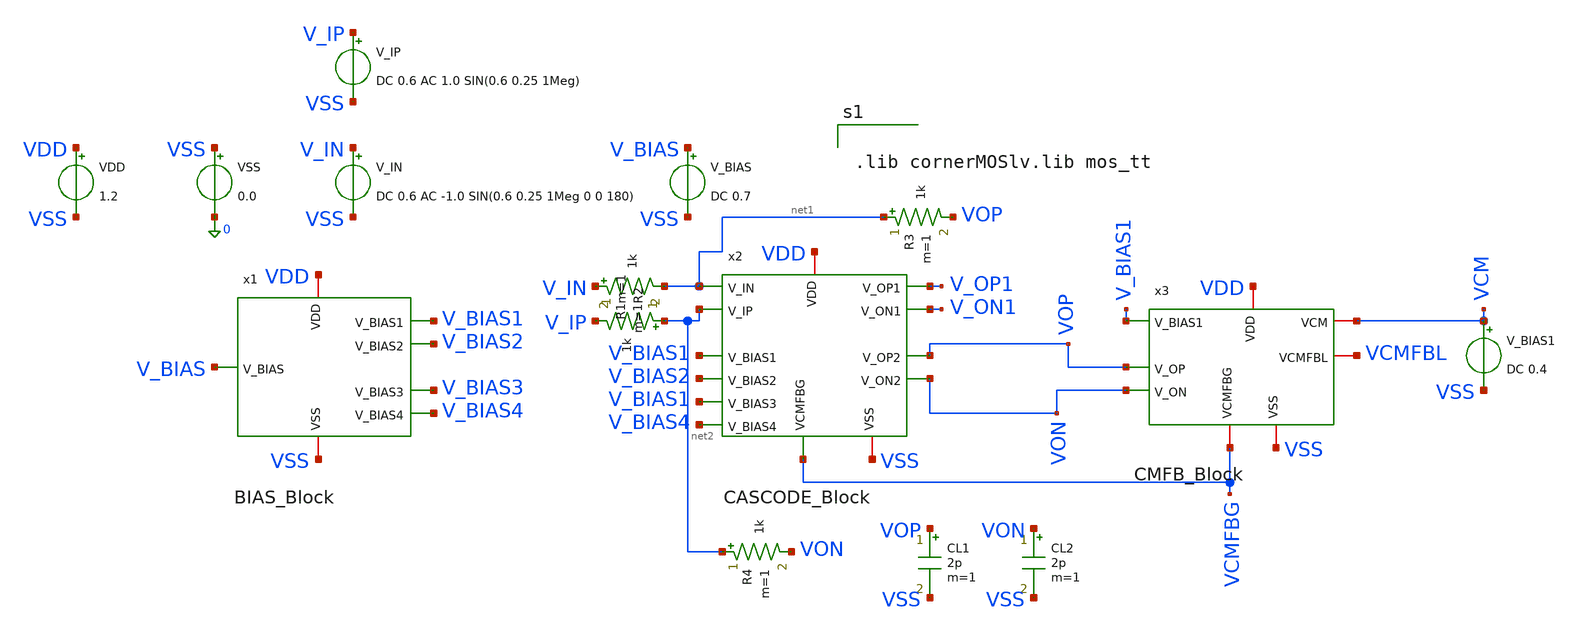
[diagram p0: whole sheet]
** sch_path: two-stage-ota-with-cmfb/Simulation/TEST_TRANS.sch
**.subckt TEST_TRANS
VDD VDD VSS 1.2
VSS VSS 0 0.0
V_IN V_IN VSS DC 0.6 AC -1.0 SIN(0.6 0.25 1Meg 0 0 180)
V_IP V_IP VSS DC 0.6 AC 1.0 SIN(0.6 0.25 1Meg)
V_BIAS V_BIAS VSS DC 0.7
V_BIAS1 VCM VSS DC 0.4
CL1 VOP VSS 2p m=1
x1 VSS V_BIAS4 V_BIAS2 V_BIAS3 VDD V_BIAS1 V_BIAS BIAS_Block
x2 VDD V_BIAS1 net1 net2 V_BIAS2 V_ON1 V_OP1 V_BIAS1 VON VOP VCMFBG V_BIAS4 VSS CASCODE_Block
x3 VDD V_BIAS1 VCM VOP VON VCMFBL VCMFBG VSS CMFB_Block
CL2 VON VSS 2p m=1
R1 V_IN net1 1k m=1
R2 net2 V_IP 1k m=1
R3 net1 VOP 1k m=1
R4 net2 VON 1k m=1
**** begin user architecture code


.lib cornerMOSlv.lib mos_tt




* RUN STEP RESPONSE
.control
set color0=white
set color1=black

* Xung buoc nhay 0.5Vpp
alter @v_ip[pulse] = [ 0.475 0.725 10n 0.1n 0.1n 50n 100n ]
alter @v_in[pulse] = [ 0.725 0.475 10n 0.1n 0.1n 50n 100n ]

tran 20p 120n

let v_out_diff = v(vop) - v(von)
let v_in_diff  = v(v_ip) - v(v_in)
let sr_trace   = deriv(v_out_diff) / 1e6

* Do Slew Rate 20% - 80%
meas tran t_r20 when v_out_diff=-0.15 rise=1
meas tran t_r80 when v_out_diff=0.15 rise=1
let sr_rise = (0.3 / (t_r80 - t_r20)) / 1e6

meas tran t_f80 when v_out_diff=0.15 fall=1
meas tran t_f20 when v_out_diff=-0.15 fall=1
let sr_fall = (0.3 / (t_f20 - t_f80)) / 1e6

* Do Overshoot
meas tran v_max max v_out_diff from=10n to=60n
let overshoot_pct = ((v_max - 0.25) / 0.25) * 100

* Do Settling Time
meas tran t_settle_1pct when v_out_diff=0.2475 rise=1
meas tran t_settle_01pct when v_out_diff=0.24975 rise=1

print sr_rise sr_fall
print overshoot_pct
print t_settle_1pct t_settle_01pct

plot v_in_diff v_out_diff ylabel 'Voltage (V)' xlabel 'Time (s)' title 'Large-Signal Step Response'
plot sr_trace ylabel 'Slew Rate (V/us)' xlabel 'Time (s)' title 'Instantaneous Slew Rate'
.endc


**** end user architecture code
**.ends
.end
